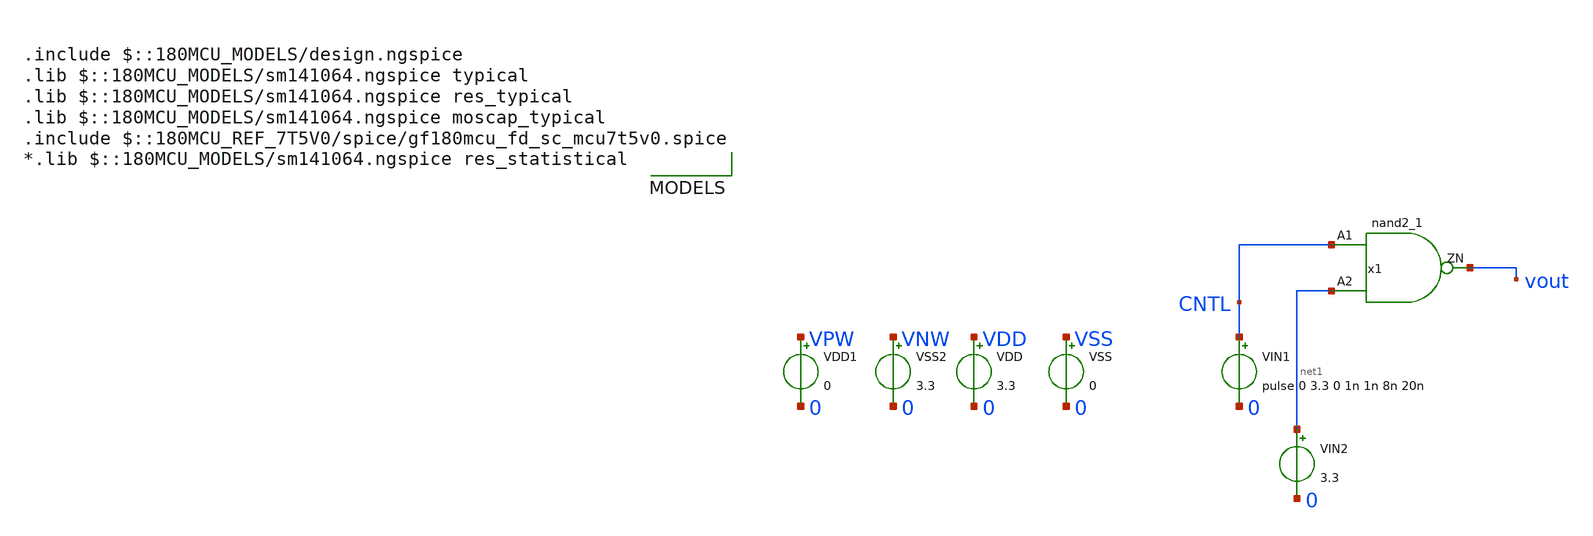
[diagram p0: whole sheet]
** sch_path: DAC/xschem/std_cell/tb_fiiles/Test_nand2.sch
**.subckt Test_nand2
VIN1 CNTL 0 pulse 0 3.3 0 1n 1n 8n 20n
VIN2 net1 0 3.3
VDD VDD 0 3.3
VSS VSS 0 0
VDD1 VPW 0 0
VSS2 VNW 0 3.3
x1 CNTL net1 vout VDD VNW VPW VSS gf180mcu_fd_sc_mcu7t5v0__nand2_1
**** begin user architecture code




.control
	tran 0.1n 50n
	*dc vin1 0 3.3 0.1
	plot v(CNTL) V(vout)
	plot v(vout)
	write test_and.raw

.endc
.save all





.include $::180MCU_MODELS/design.ngspice
.lib $::180MCU_MODELS/sm141064.ngspice typical
.lib $::180MCU_MODELS/sm141064.ngspice res_typical
.lib $::180MCU_MODELS/sm141064.ngspice moscap_typical
.include $::180MCU_REF_7T5V0/spice/gf180mcu_fd_sc_mcu7t5v0.spice
*.lib $::180MCU_MODELS/sm141064.ngspice res_statistical

**** end user architecture code
**.ends
.end
